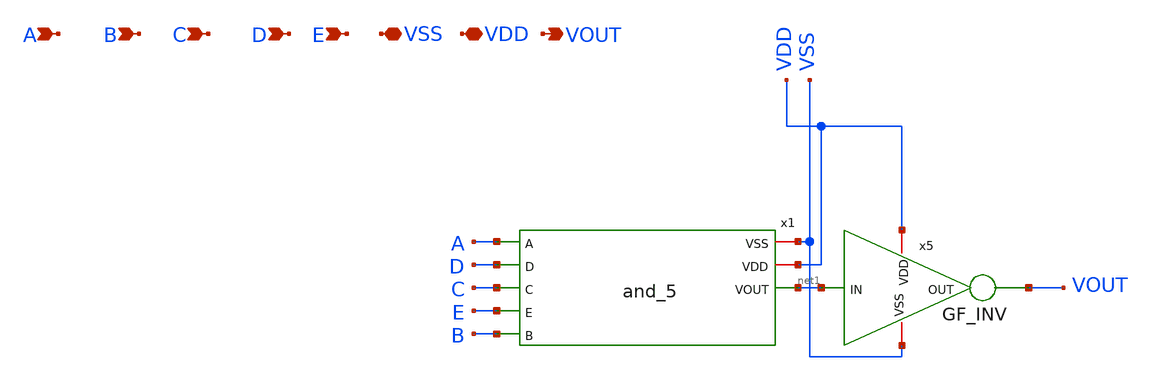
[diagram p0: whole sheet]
** sch_path: Clock_Generator_PAKISTAN_02/xschem/nand_5.sch
**.subckt nand_5 B VSS VDD A VOUT D C E
*.ipin B
*.iopin VSS
*.iopin VDD
*.ipin A
*.opin VOUT
*.ipin D
*.ipin C
*.ipin E
x5 VSS VDD VOUT net1 GF_INV
x1 VSS VDD A net1 D C E B and_5
**.ends
.end
